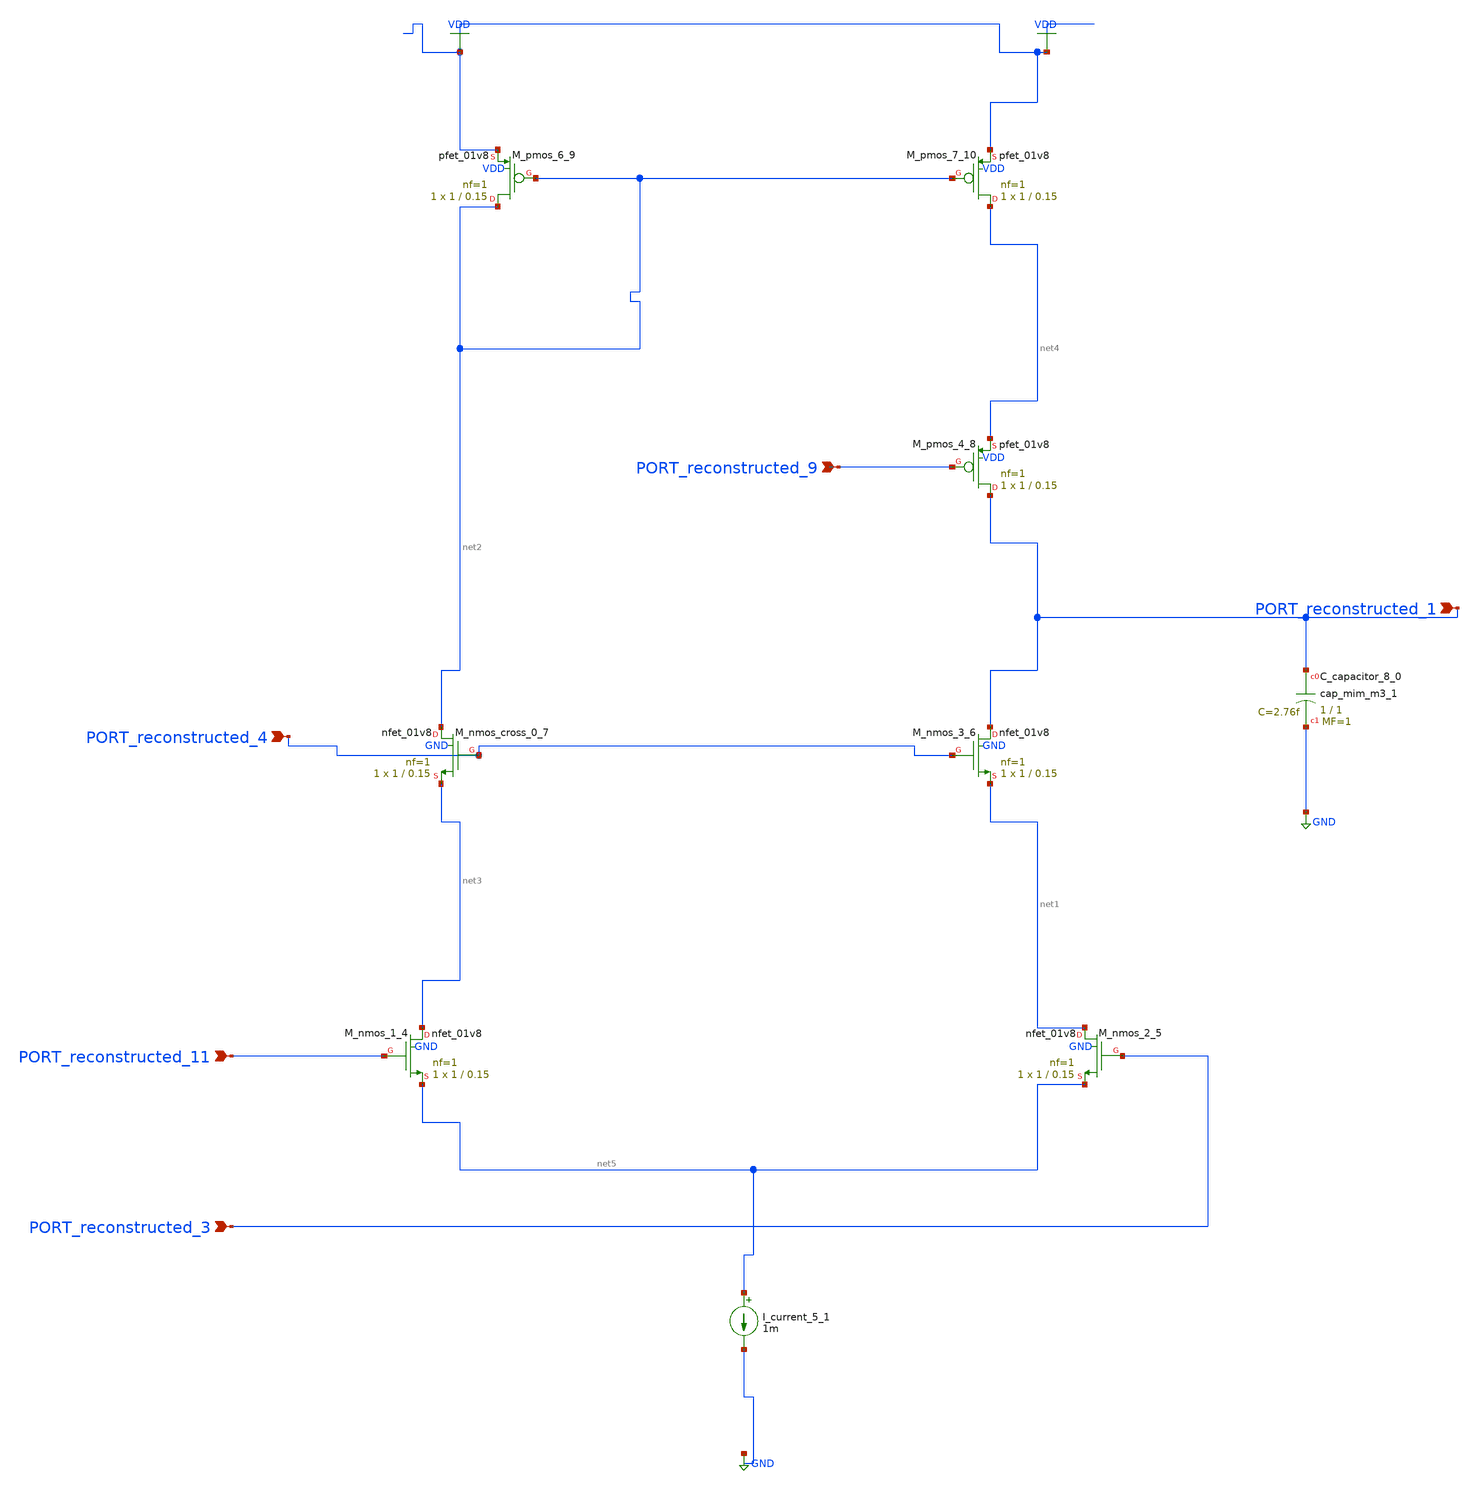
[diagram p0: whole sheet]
** sch_path: schematics/AMSNet/719.sch
**.subckt 719 PORT_reconstructed_9 PORT_reconstructed_4 PORT_reconstructed_11 PORT_reconstructed_3
*+ PORT_reconstructed_1
*.ipin PORT_reconstructed_9
*.ipin PORT_reconstructed_4
*.ipin PORT_reconstructed_11
*.ipin PORT_reconstructed_3
*.ipin PORT_reconstructed_1
XC_capacitor_8_0 PORT_reconstructed_1 GND sky130_fd_pr__cap_mim_m3_1 W=1 L=1 MF=1 m=1
I_current_5_1 net5 GND 1m
XM_nmos_1_4 net3 PORT_reconstructed_11 net5 GND sky130_fd_pr__nfet_01v8 L=0.15 W=1 nf=1 ad='int((1 + 1)/2) * 1 / 1 * 0.29'
+ as='int((1 + 2)/2) * 1 / 1 * 0.29' pd='2*int((1 + 1)/2) * (1 / 1 + 0.29)' ps='2*int((1 + 2)/2) * (1 / 1 + 0.29)'
+ nrd='0.29 / 1 ' nrs='0.29 / 1 ' sa=0 sb=0 sd=0 mult=1 m=1
XM_nmos_2_5 net1 PORT_reconstructed_3 net5 GND sky130_fd_pr__nfet_01v8 L=0.15 W=1 nf=1 ad='int((1 + 1)/2) * 1 / 1 * 0.29'
+ as='int((1 + 2)/2) * 1 / 1 * 0.29' pd='2*int((1 + 1)/2) * (1 / 1 + 0.29)' ps='2*int((1 + 2)/2) * (1 / 1 + 0.29)'
+ nrd='0.29 / 1 ' nrs='0.29 / 1 ' sa=0 sb=0 sd=0 mult=1 m=1
XM_nmos_3_6 PORT_reconstructed_1 PORT_reconstructed_4 net1 GND sky130_fd_pr__nfet_01v8 L=0.15 W=1 nf=1
+ ad='int((1 + 1)/2) * 1 / 1 * 0.29' as='int((1 + 2)/2) * 1 / 1 * 0.29' pd='2*int((1 + 1)/2) * (1 / 1 + 0.29)'
+ ps='2*int((1 + 2)/2) * (1 / 1 + 0.29)' nrd='0.29 / 1 ' nrs='0.29 / 1 ' sa=0 sb=0 sd=0 mult=1 m=1
XM_nmos_cross_0_7 net2 PORT_reconstructed_4 net3 GND sky130_fd_pr__nfet_01v8 L=0.15 W=1 nf=1 ad='int((1 + 1)/2) * 1 / 1 * 0.29'
+ as='int((1 + 2)/2) * 1 / 1 * 0.29' pd='2*int((1 + 1)/2) * (1 / 1 + 0.29)' ps='2*int((1 + 2)/2) * (1 / 1 + 0.29)'
+ nrd='0.29 / 1 ' nrs='0.29 / 1 ' sa=0 sb=0 sd=0 mult=1 m=1
XM_pmos_4_8 PORT_reconstructed_1 PORT_reconstructed_9 net4 VDD sky130_fd_pr__pfet_01v8 L=0.15 W=1 nf=1
+ ad='int((1 + 1)/2) * 1 / 1 * 0.29' as='int((1 + 2)/2) * 1 / 1 * 0.29' pd='2*int((1 + 1)/2) * (1 / 1 + 0.29)'
+ ps='2*int((1 + 2)/2) * (1 / 1 + 0.29)' nrd='0.29 / 1 ' nrs='0.29 / 1 ' sa=0 sb=0 sd=0 mult=1 m=1
XM_pmos_6_9 net2 net2 VDD VDD sky130_fd_pr__pfet_01v8 L=0.15 W=1 nf=1 ad='int((1 + 1)/2) * 1 / 1 * 0.29'
+ as='int((1 + 2)/2) * 1 / 1 * 0.29' pd='2*int((1 + 1)/2) * (1 / 1 + 0.29)' ps='2*int((1 + 2)/2) * (1 / 1 + 0.29)'
+ nrd='0.29 / 1 ' nrs='0.29 / 1 ' sa=0 sb=0 sd=0 mult=1 m=1
XM_pmos_7_10 net4 net2 VDD VDD sky130_fd_pr__pfet_01v8 L=0.15 W=1 nf=1 ad='int((1 + 1)/2) * 1 / 1 * 0.29'
+ as='int((1 + 2)/2) * 1 / 1 * 0.29' pd='2*int((1 + 1)/2) * (1 / 1 + 0.29)' ps='2*int((1 + 2)/2) * (1 / 1 + 0.29)'
+ nrd='0.29 / 1 ' nrs='0.29 / 1 ' sa=0 sb=0 sd=0 mult=1 m=1
**.ends
.GLOBAL GND
.GLOBAL VDD
.end
